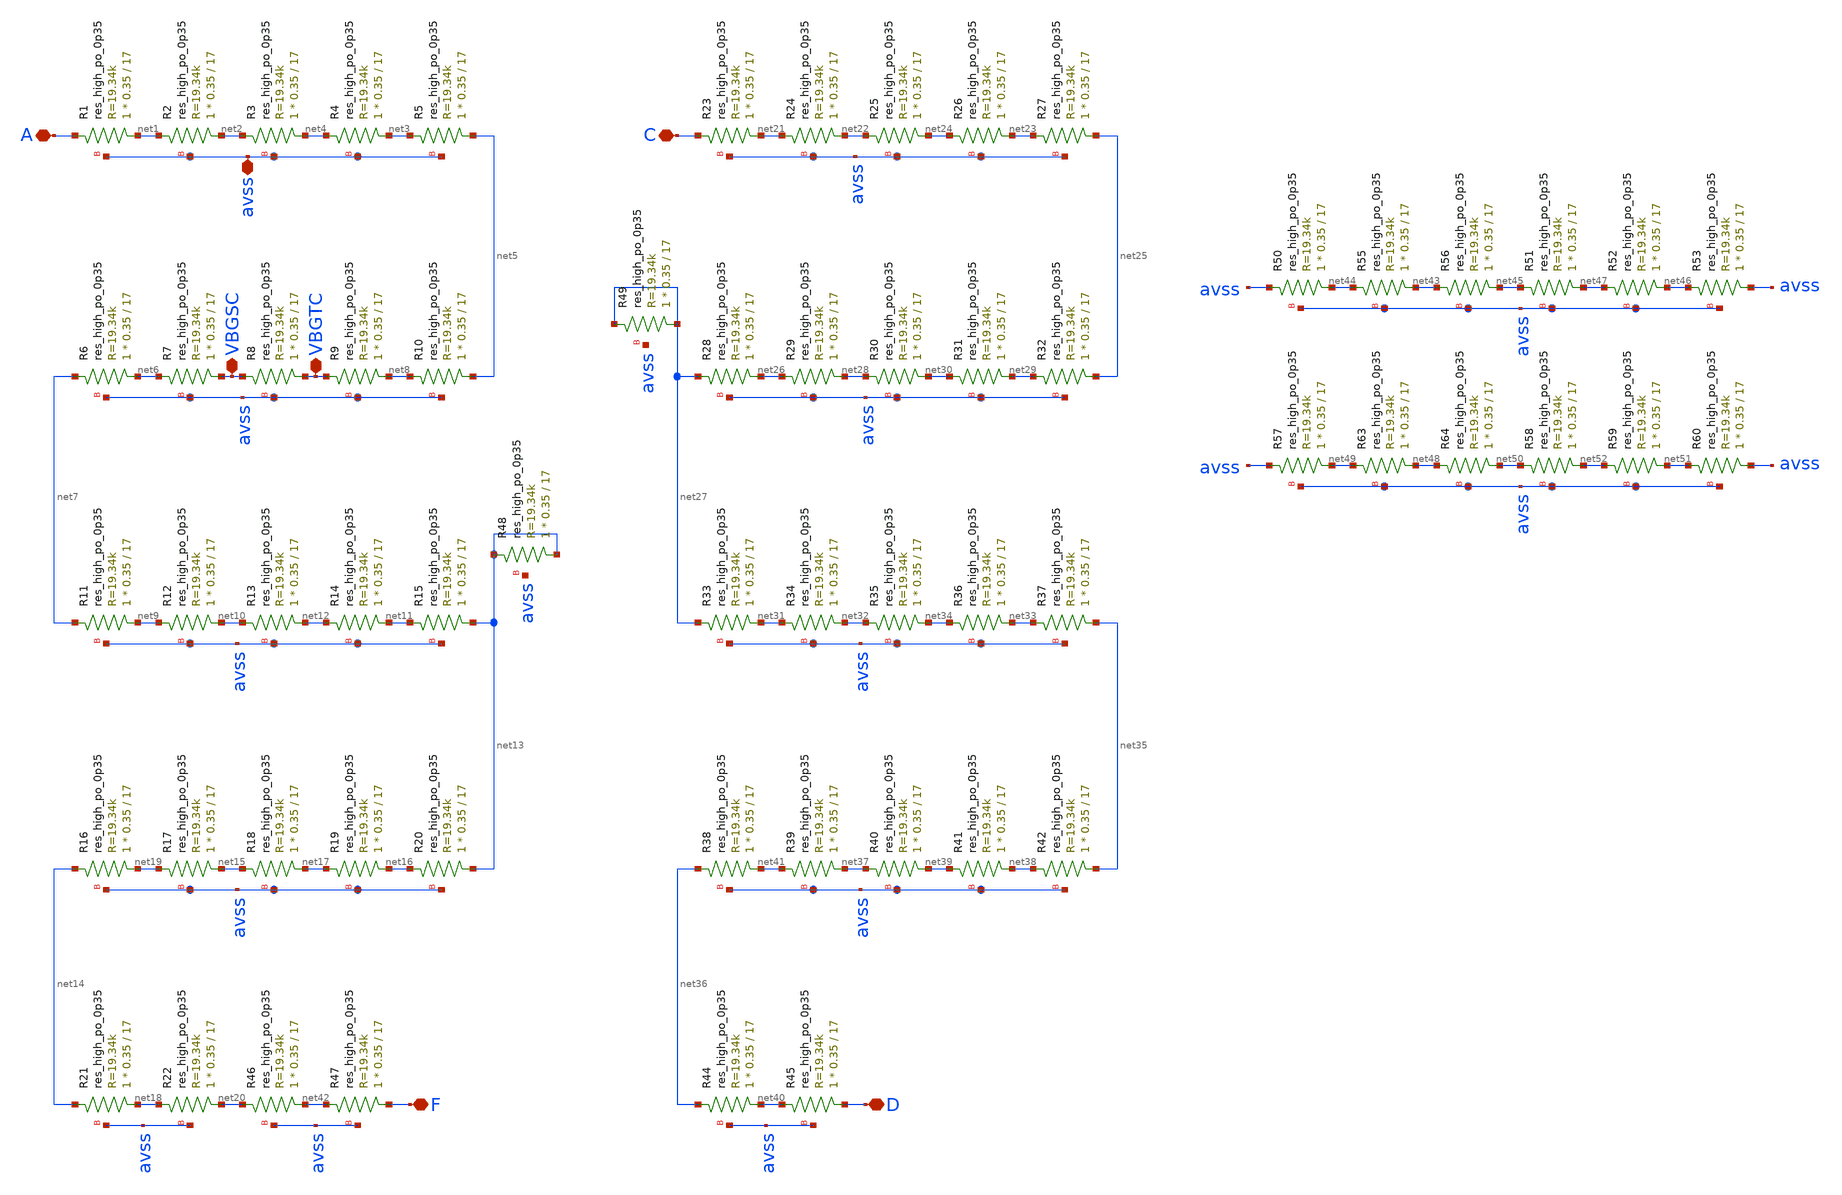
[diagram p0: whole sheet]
** sch_path: magic/resist_const.sch
**.subckt resist_const A VBGTC VBGSC avss C D F
*.iopin A
*.iopin VBGTC
*.iopin VBGSC
*.iopin avss
*.iopin C
*.iopin D
*.iopin F
XR1 net1 A avss sky130_fd_pr__res_high_po_0p35 L=17 mult=1 m=1
XR2 net2 net1 avss sky130_fd_pr__res_high_po_0p35 L=17 mult=1 m=1
XR3 net4 net2 avss sky130_fd_pr__res_high_po_0p35 L=17 mult=1 m=1
XR4 net3 net4 avss sky130_fd_pr__res_high_po_0p35 L=17 mult=1 m=1
XR5 net5 net3 avss sky130_fd_pr__res_high_po_0p35 L=17 mult=1 m=1
XR8 VBGTC VBGSC avss sky130_fd_pr__res_high_po_0p35 L=17 mult=1 m=1
XR9 net8 VBGTC avss sky130_fd_pr__res_high_po_0p35 L=17 mult=1 m=1
XR10 net5 net8 avss sky130_fd_pr__res_high_po_0p35 L=17 mult=1 m=1
XR12 net10 net9 avss sky130_fd_pr__res_high_po_0p35 L=17 mult=1 m=1
XR13 net12 net10 avss sky130_fd_pr__res_high_po_0p35 L=17 mult=1 m=1
XR14 net11 net12 avss sky130_fd_pr__res_high_po_0p35 L=17 mult=1 m=1
XR15 net13 net11 avss sky130_fd_pr__res_high_po_0p35 L=17 mult=1 m=1
XR17 net15 net19 avss sky130_fd_pr__res_high_po_0p35 L=17 mult=1 m=1
XR18 net17 net15 avss sky130_fd_pr__res_high_po_0p35 L=17 mult=1 m=1
XR19 net16 net17 avss sky130_fd_pr__res_high_po_0p35 L=17 mult=1 m=1
XR20 net13 net16 avss sky130_fd_pr__res_high_po_0p35 L=17 mult=1 m=1
XR22 net20 net18 avss sky130_fd_pr__res_high_po_0p35 L=17 mult=1 m=1
XR23 net21 C avss sky130_fd_pr__res_high_po_0p35 L=17 mult=1 m=1
XR24 net22 net21 avss sky130_fd_pr__res_high_po_0p35 L=17 mult=1 m=1
XR25 net24 net22 avss sky130_fd_pr__res_high_po_0p35 L=17 mult=1 m=1
XR26 net23 net24 avss sky130_fd_pr__res_high_po_0p35 L=17 mult=1 m=1
XR27 net25 net23 avss sky130_fd_pr__res_high_po_0p35 L=17 mult=1 m=1
XR30 net30 net28 avss sky130_fd_pr__res_high_po_0p35 L=17 mult=1 m=1
XR31 net29 net30 avss sky130_fd_pr__res_high_po_0p35 L=17 mult=1 m=1
XR32 net25 net29 avss sky130_fd_pr__res_high_po_0p35 L=17 mult=1 m=1
XR33 net31 net27 avss sky130_fd_pr__res_high_po_0p35 L=17 mult=1 m=1
XR34 net32 net31 avss sky130_fd_pr__res_high_po_0p35 L=17 mult=1 m=1
XR35 net34 net32 avss sky130_fd_pr__res_high_po_0p35 L=17 mult=1 m=1
XR36 net33 net34 avss sky130_fd_pr__res_high_po_0p35 L=17 mult=1 m=1
XR37 net35 net33 avss sky130_fd_pr__res_high_po_0p35 L=17 mult=1 m=1
XR39 net37 net41 avss sky130_fd_pr__res_high_po_0p35 L=17 mult=1 m=1
XR40 net39 net37 avss sky130_fd_pr__res_high_po_0p35 L=17 mult=1 m=1
XR41 net38 net39 avss sky130_fd_pr__res_high_po_0p35 L=17 mult=1 m=1
XR42 net35 net38 avss sky130_fd_pr__res_high_po_0p35 L=17 mult=1 m=1
XR44 net40 net36 avss sky130_fd_pr__res_high_po_0p35 L=17 mult=1 m=1
XR45 D net40 avss sky130_fd_pr__res_high_po_0p35 L=17 mult=1 m=1
XR46 net42 net20 avss sky130_fd_pr__res_high_po_0p35 L=17 mult=1 m=1
XR47 F net42 avss sky130_fd_pr__res_high_po_0p35 L=17 mult=1 m=1
XR28 net26 net27 avss sky130_fd_pr__res_high_po_0p35 L=17 mult=1 m=1
XR6 net6 net7 avss sky130_fd_pr__res_high_po_0p35 L=17 mult=1 m=1
XR16 net19 net14 avss sky130_fd_pr__res_high_po_0p35 L=17 mult=1 m=1
XR11 net9 net7 avss sky130_fd_pr__res_high_po_0p35 L=17 mult=1 m=1
XR21 net18 net14 avss sky130_fd_pr__res_high_po_0p35 L=17 mult=1 m=1
XR38 net41 net36 avss sky130_fd_pr__res_high_po_0p35 L=17 mult=1 m=1
XR29 net28 net26 avss sky130_fd_pr__res_high_po_0p35 L=17 mult=1 m=1
XR7 VBGSC net6 avss sky130_fd_pr__res_high_po_0p35 L=17 mult=1 m=1
XR48 net13 net13 avss sky130_fd_pr__res_high_po_0p35 L=17 mult=1 m=1
XR49 net27 net27 avss sky130_fd_pr__res_high_po_0p35 L=17 mult=1 m=1
XR50 net44 avss avss sky130_fd_pr__res_high_po_0p35 L=17 mult=1 m=1
XR51 net47 net45 avss sky130_fd_pr__res_high_po_0p35 L=17 mult=1 m=1
XR52 net46 net47 avss sky130_fd_pr__res_high_po_0p35 L=17 mult=1 m=1
XR53 avss net46 avss sky130_fd_pr__res_high_po_0p35 L=17 mult=1 m=1
XR55 net43 net44 avss sky130_fd_pr__res_high_po_0p35 L=17 mult=1 m=1
XR56 net45 net43 avss sky130_fd_pr__res_high_po_0p35 L=17 mult=1 m=1
XR57 net49 avss avss sky130_fd_pr__res_high_po_0p35 L=17 mult=1 m=1
XR58 net52 net50 avss sky130_fd_pr__res_high_po_0p35 L=17 mult=1 m=1
XR59 net51 net52 avss sky130_fd_pr__res_high_po_0p35 L=17 mult=1 m=1
XR60 avss net51 avss sky130_fd_pr__res_high_po_0p35 L=17 mult=1 m=1
XR63 net48 net49 avss sky130_fd_pr__res_high_po_0p35 L=17 mult=1 m=1
XR64 net50 net48 avss sky130_fd_pr__res_high_po_0p35 L=17 mult=1 m=1
**.ends
.end
